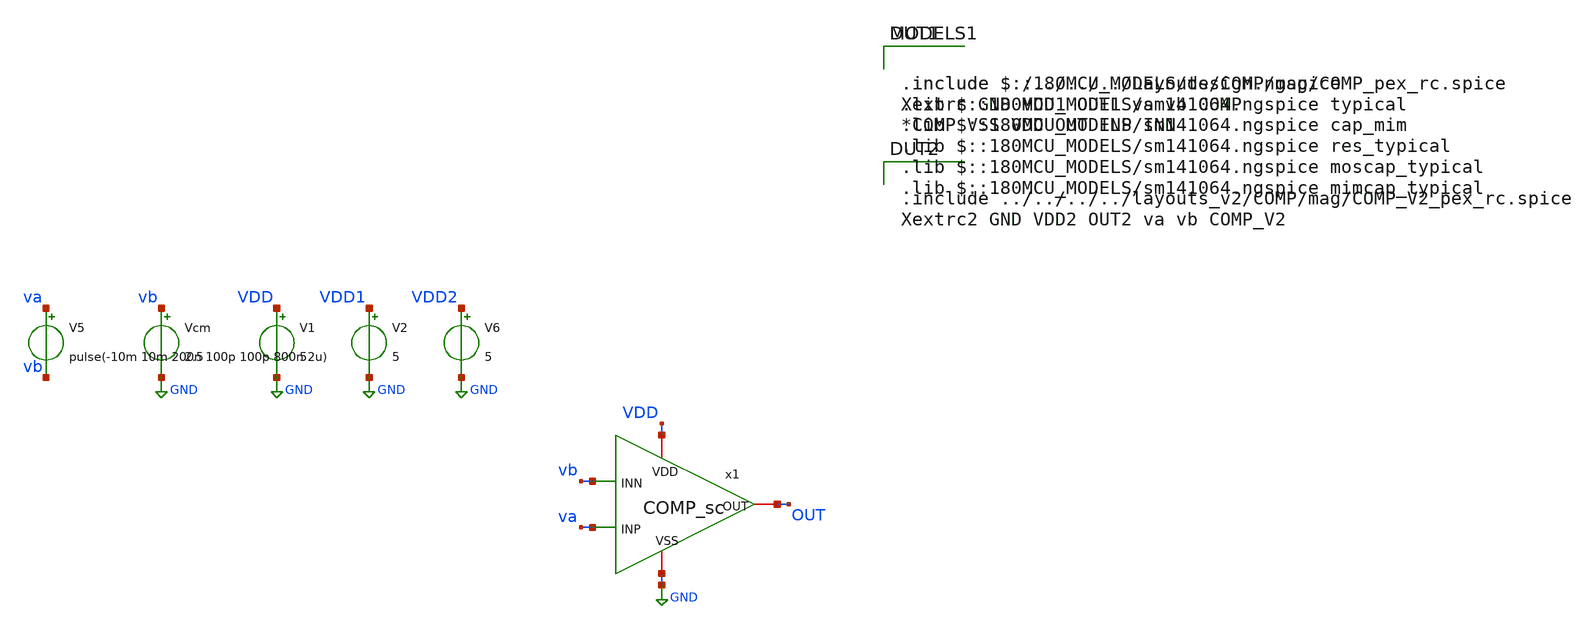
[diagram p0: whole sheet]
** sch_path: FINAL/XSCHEM/TEST/test_comp_tran.sch
**.subckt test_comp_tran
V1 VDD GND 5
V2 VDD1 GND 5
V5 va vb pulse(-10m 10m 200n 100p 100p 800n 2u)
Vcm vb GND 2.5
x1 VDD vb OUT va GND COMP_sc
V6 VDD2 GND 5
**** begin user architecture code

.include $::180MCU_MODELS/design.ngspice
.lib $::180MCU_MODELS/sm141064.ngspice typical
.lib $::180MCU_MODELS/sm141064.ngspice cap_mim
.lib $::180MCU_MODELS/sm141064.ngspice res_typical
.lib $::180MCU_MODELS/sm141064.ngspice moscap_typical
.lib $::180MCU_MODELS/sm141064.ngspice mimcap_typical


.include ../../../../Layouts/COMP/mag/COMP_pex_rc.spice
Xextrc GND VDD1 OUT1 va vb COMP
*COMP VSS VDD OUT INP INN


.include ../../../../layouts_v2/COMP/mag/COMP_V2_pex_rc.spice
Xextrc2 GND VDD2 OUT2 va vb COMP_V2



* OJO: ni una llave en este texto. xschem las cuenta para saber donde acaba el
* bloque de atributos y una sola dentro de un comentario lo corta por la mitad,
* dejando el netlist con el 'blabla' de la plantilla y sin dar ningun error.
*
* Transitorio de comparador, no de amplificador: lazo abierto y un escalon de
* sobreexcitacion de +-10 mV alrededor del umbral. Lo que se mide es el retardo
* de propagacion -- del cruce de la entrada al cruce de medio rail de la
* salida -- y los tiempos de subida y de bajada, para el esquematico y para el
* layout extraido.
* El umbral es cero porque el offset medido del COMP es de decimas de milivoltio.
.save all
.control
tran 200p 2u
wrdata tran.txt v(va)-v(vb) v(OUT) v(OUT1) v(OUT2)
.endc


**** end user architecture code
**.ends
.GLOBAL GND
.end
